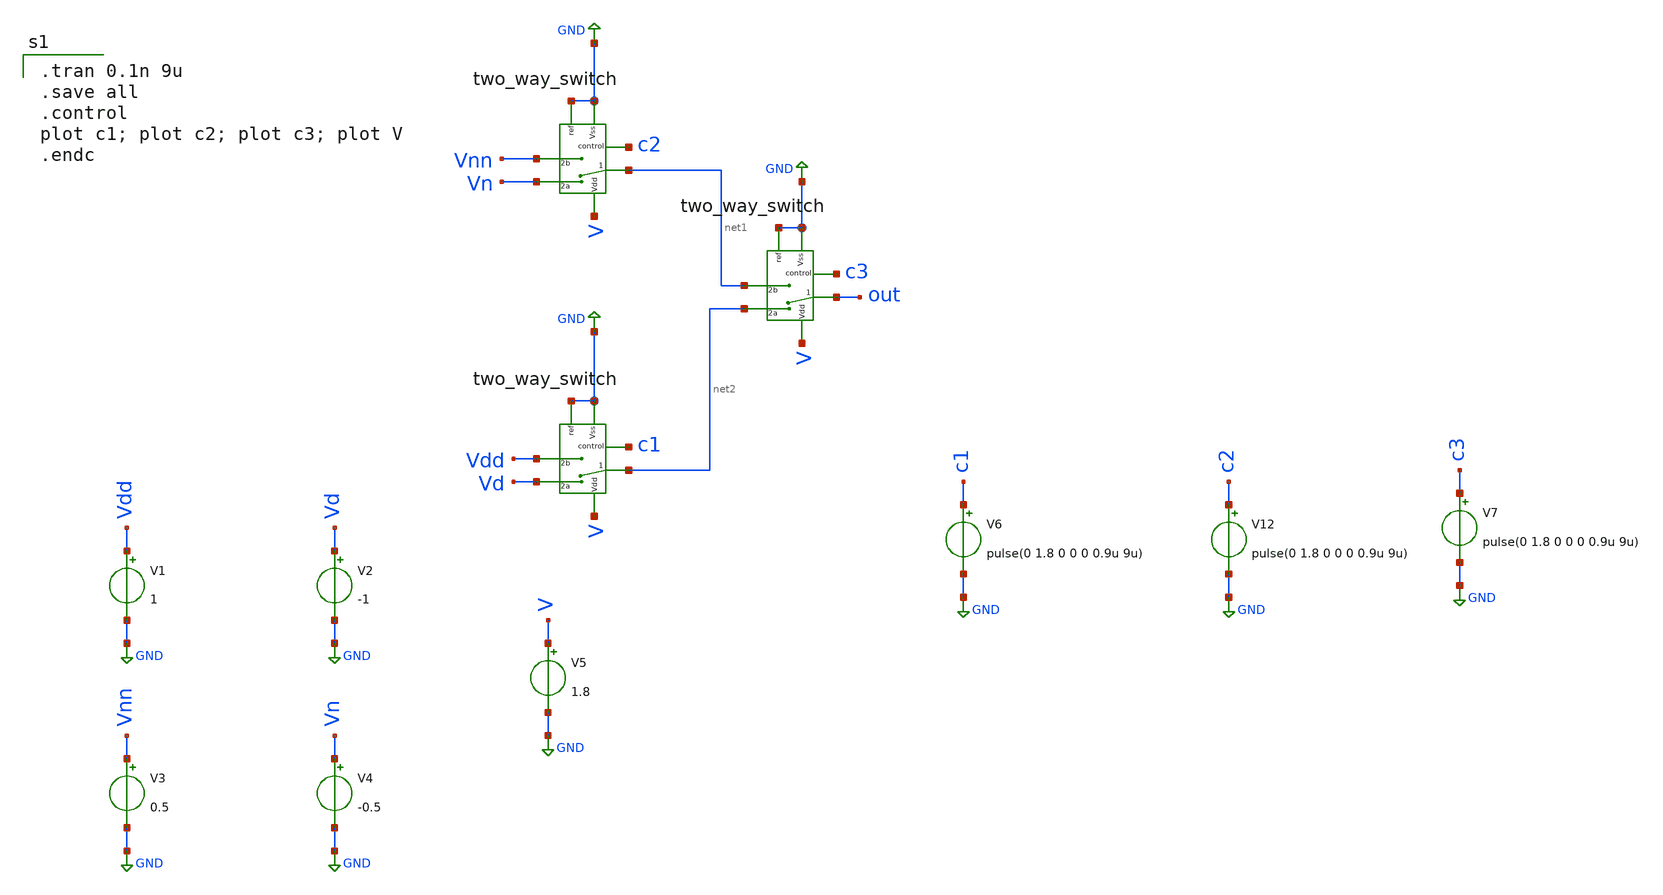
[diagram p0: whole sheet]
** sch_path: Behavioral_model/test.sch
**.subckt test
x26 net1 V c2 GND Vn Vnn GND two_way_switch
x1 out V c3 GND net2 net1 GND two_way_switch
x2 net2 V c1 GND Vd Vdd GND two_way_switch
V12 c2 GND pulse(0 1.8 0 0 0 0.9u 9u)
V1 Vdd GND 1
V2 Vd GND -1
V3 Vnn GND 0.5
V4 Vn GND -0.5
V5 V GND 1.8
V6 c1 GND pulse(0 1.8 0 0 0 0.9u 9u)
V7 c3 GND pulse(0 1.8 0 0 0 0.9u 9u)
**** begin user architecture code

.lib /usr/local/share/pdk/sky130A/libs.tech/ngspice/sky130.lib.spice tt


.model switch1 sw vt=0.1 vh=0 ron=1m roff=100G


.tran 0.1n 9u
.save all
.control
plot c1; plot c2; plot c3; plot V
.endc

**** end user architecture code
**.ends

* expanding   symbol:  two_way_switch.sym # of pins=7
** sym_path: Behavioral_model/two_way_switch.sym
** sch_path: Behavioral_model/two_way_switch.sch
.subckt two_way_switch 1 Vdd control ref 2a 2b Vss
*.iopin 2b
*.iopin 2a
*.ipin ref
*.iopin 1
*.ipin Vdd
*.ipin Vss
*.ipin control
S1 1 2a control ref SWITCH1
S2 1 2b net1 ref SWITCH1
x1 Vdd control net1 Vss CMOS_inverter
.ends


* expanding   symbol:  CMOS_inverter.sym # of pins=4
** sym_path: Behavioral_model/CMOS_inverter.sym
** sch_path: Behavioral_model/CMOS_inverter.sch
.subckt CMOS_inverter Vdd Q Q_N Vss
*.ipin Q
*.ipin Vdd
*.ipin Vss
*.opin Q_N
XM1 Q_N Q Vss Vss sky130_fd_pr__nfet_01v8 L=0.15 W=1 nf=1 ad='int((nf+1)/2) * W/nf * 0.29' as='int((nf+2)/2) * W/nf * 0.29'
+ pd='2*int((nf+1)/2) * (W/nf + 0.29)' ps='2*int((nf+2)/2) * (W/nf + 0.29)' nrd='0.29 / W' nrs='0.29 / W'
+ sa=0 sb=0 sd=0 mult=1 m=1
XM3 Q_N Q Vdd Vdd sky130_fd_pr__pfet_01v8 L=0.15 W=1 nf=1 ad='int((nf+1)/2) * W/nf * 0.29' as='int((nf+2)/2) * W/nf * 0.29'
+ pd='2*int((nf+1)/2) * (W/nf + 0.29)' ps='2*int((nf+2)/2) * (W/nf + 0.29)' nrd='0.29 / W' nrs='0.29 / W'
+ sa=0 sb=0 sd=0 mult=1 m=1
.ends

.GLOBAL GND
.end
